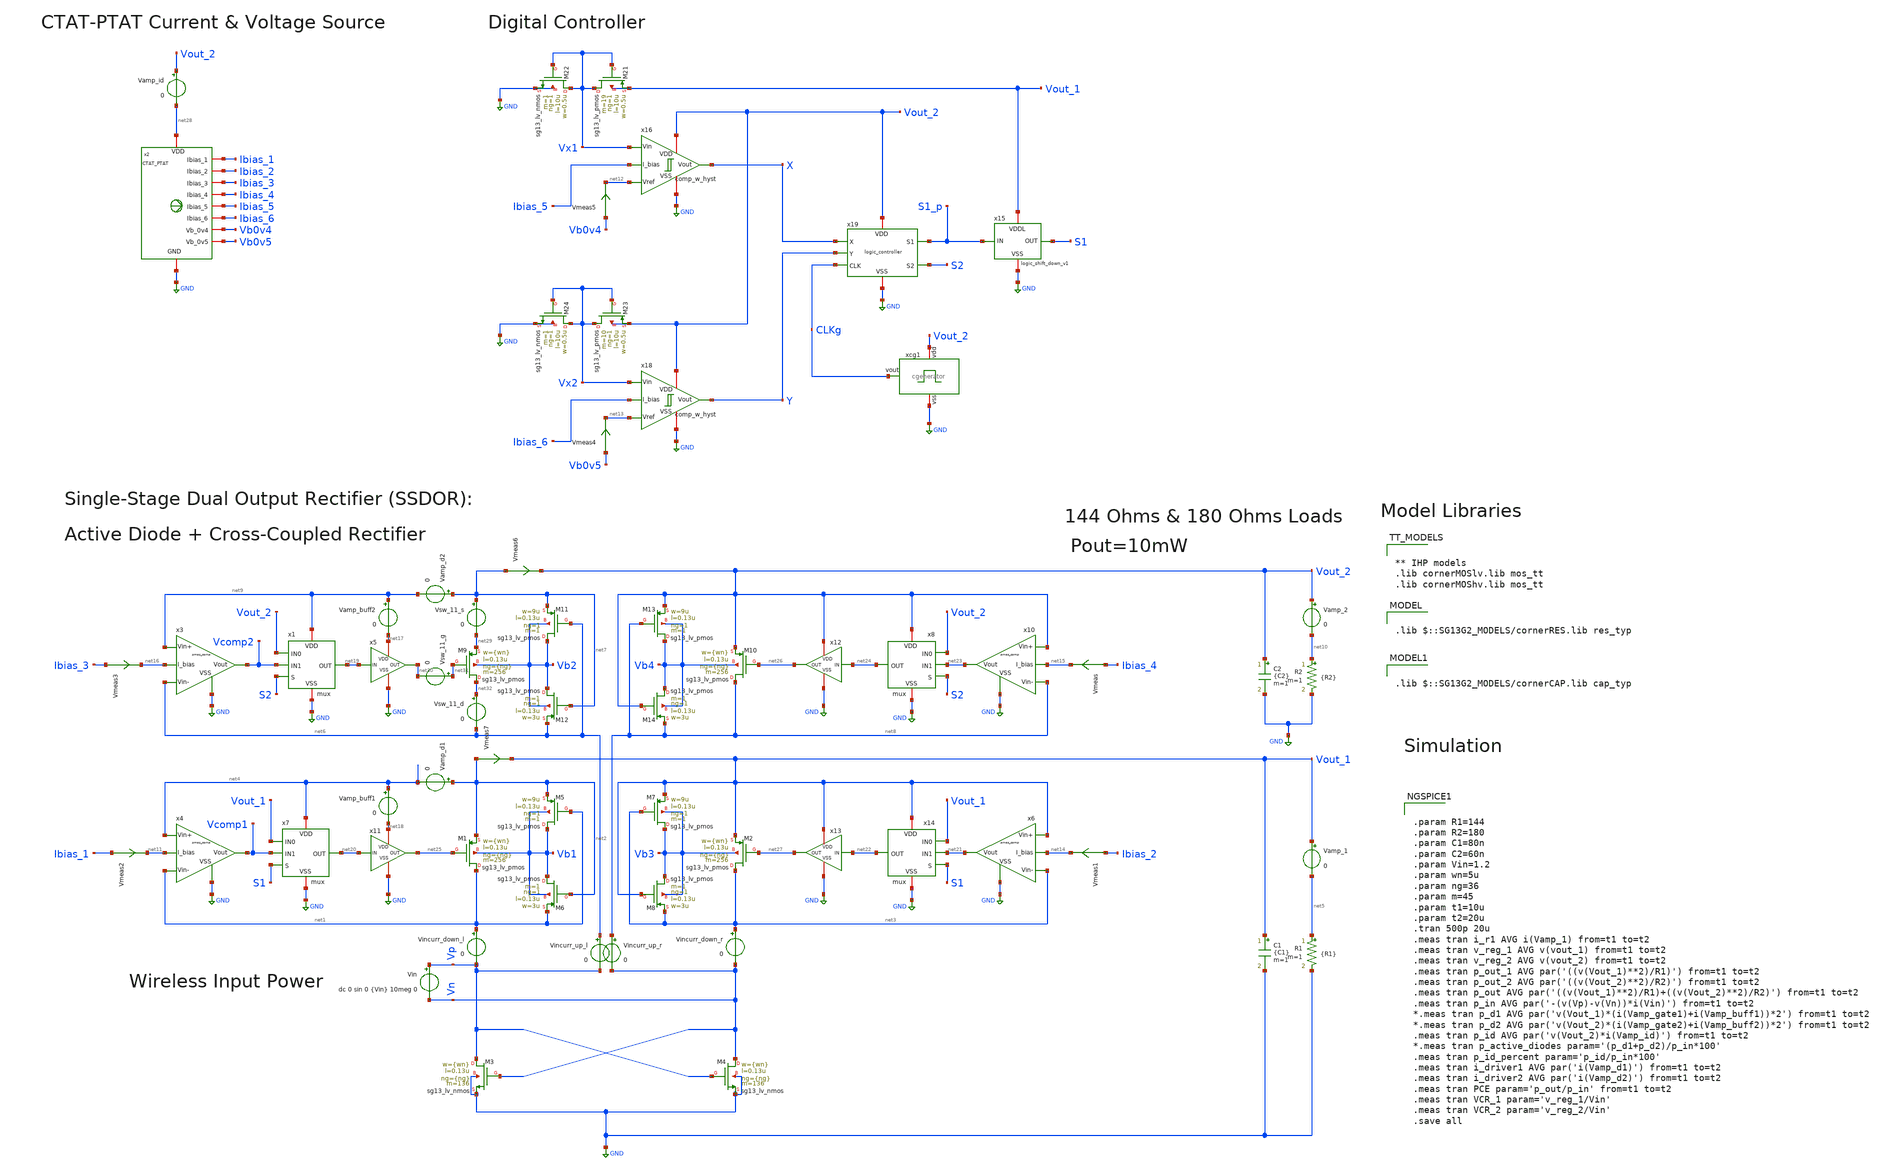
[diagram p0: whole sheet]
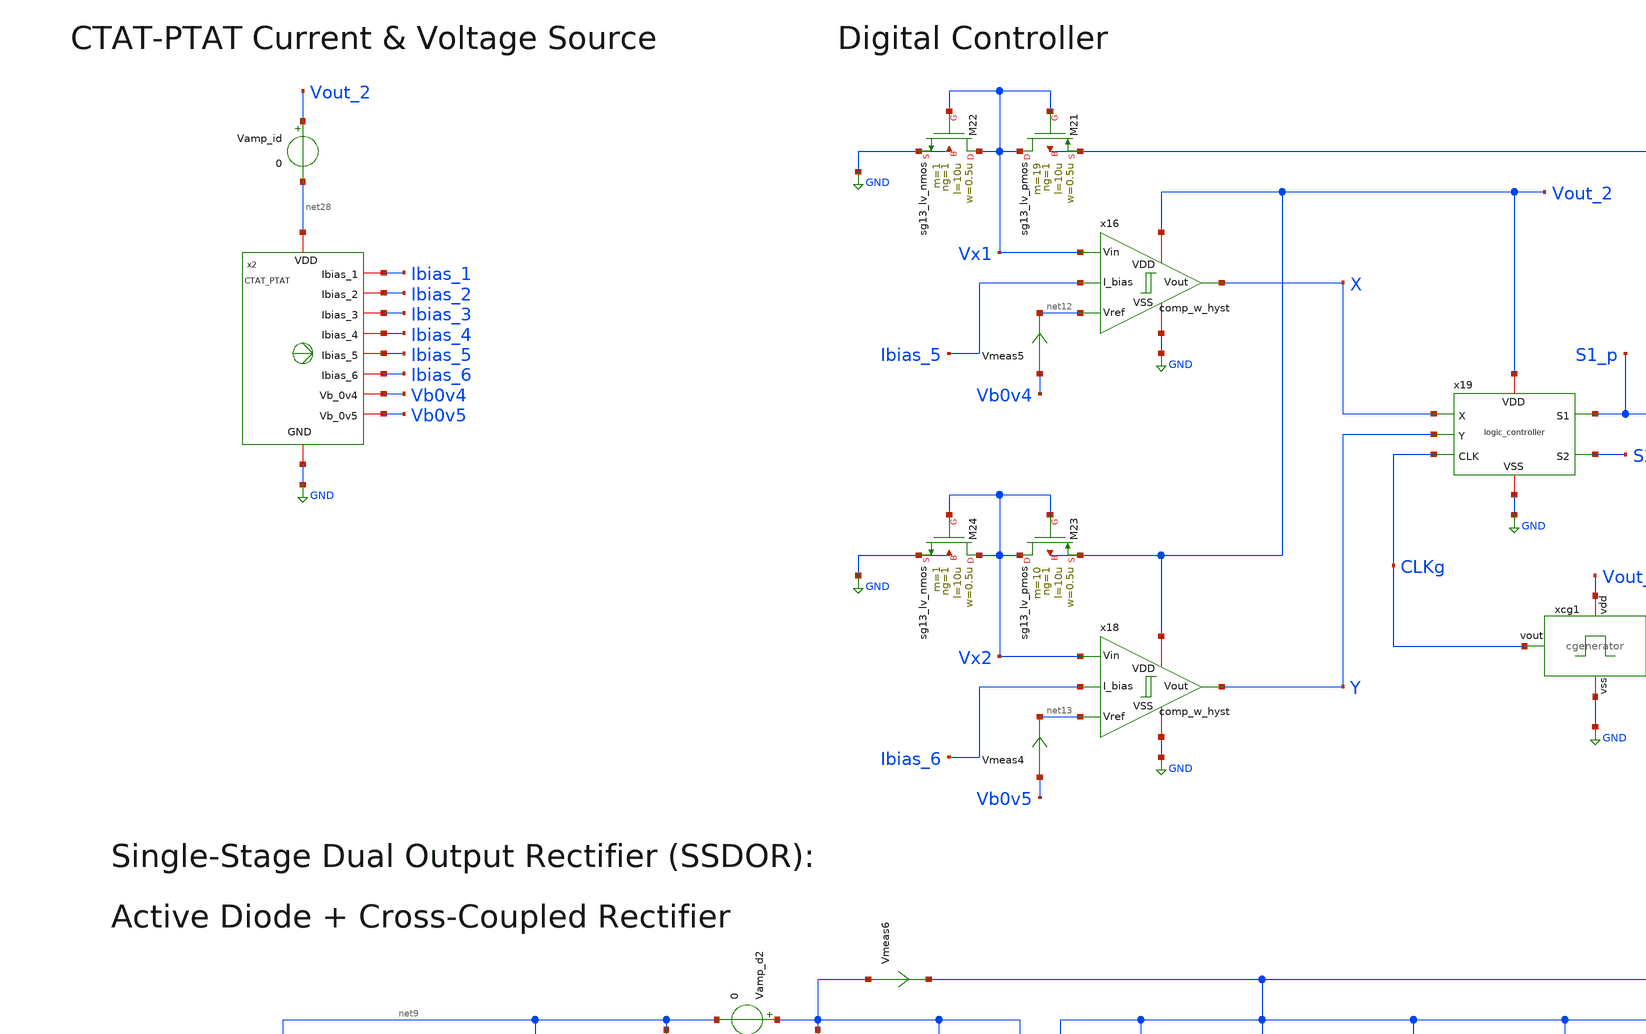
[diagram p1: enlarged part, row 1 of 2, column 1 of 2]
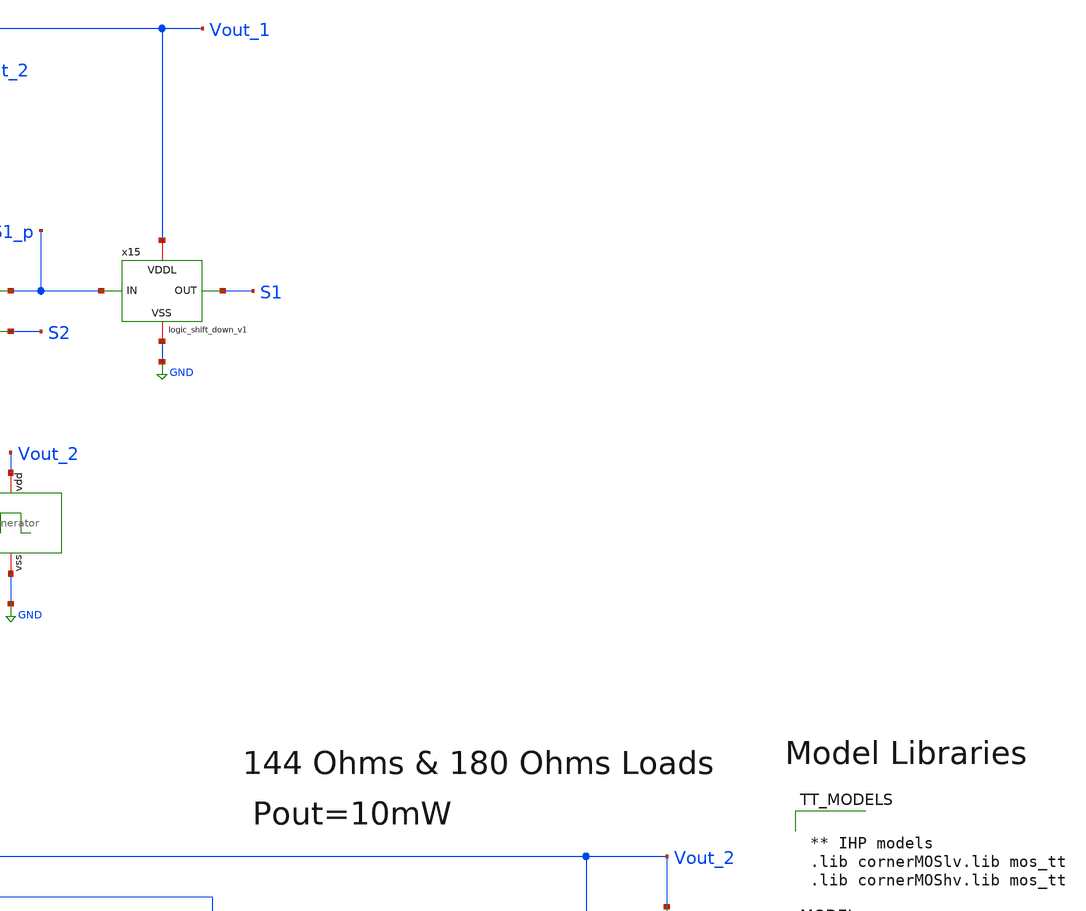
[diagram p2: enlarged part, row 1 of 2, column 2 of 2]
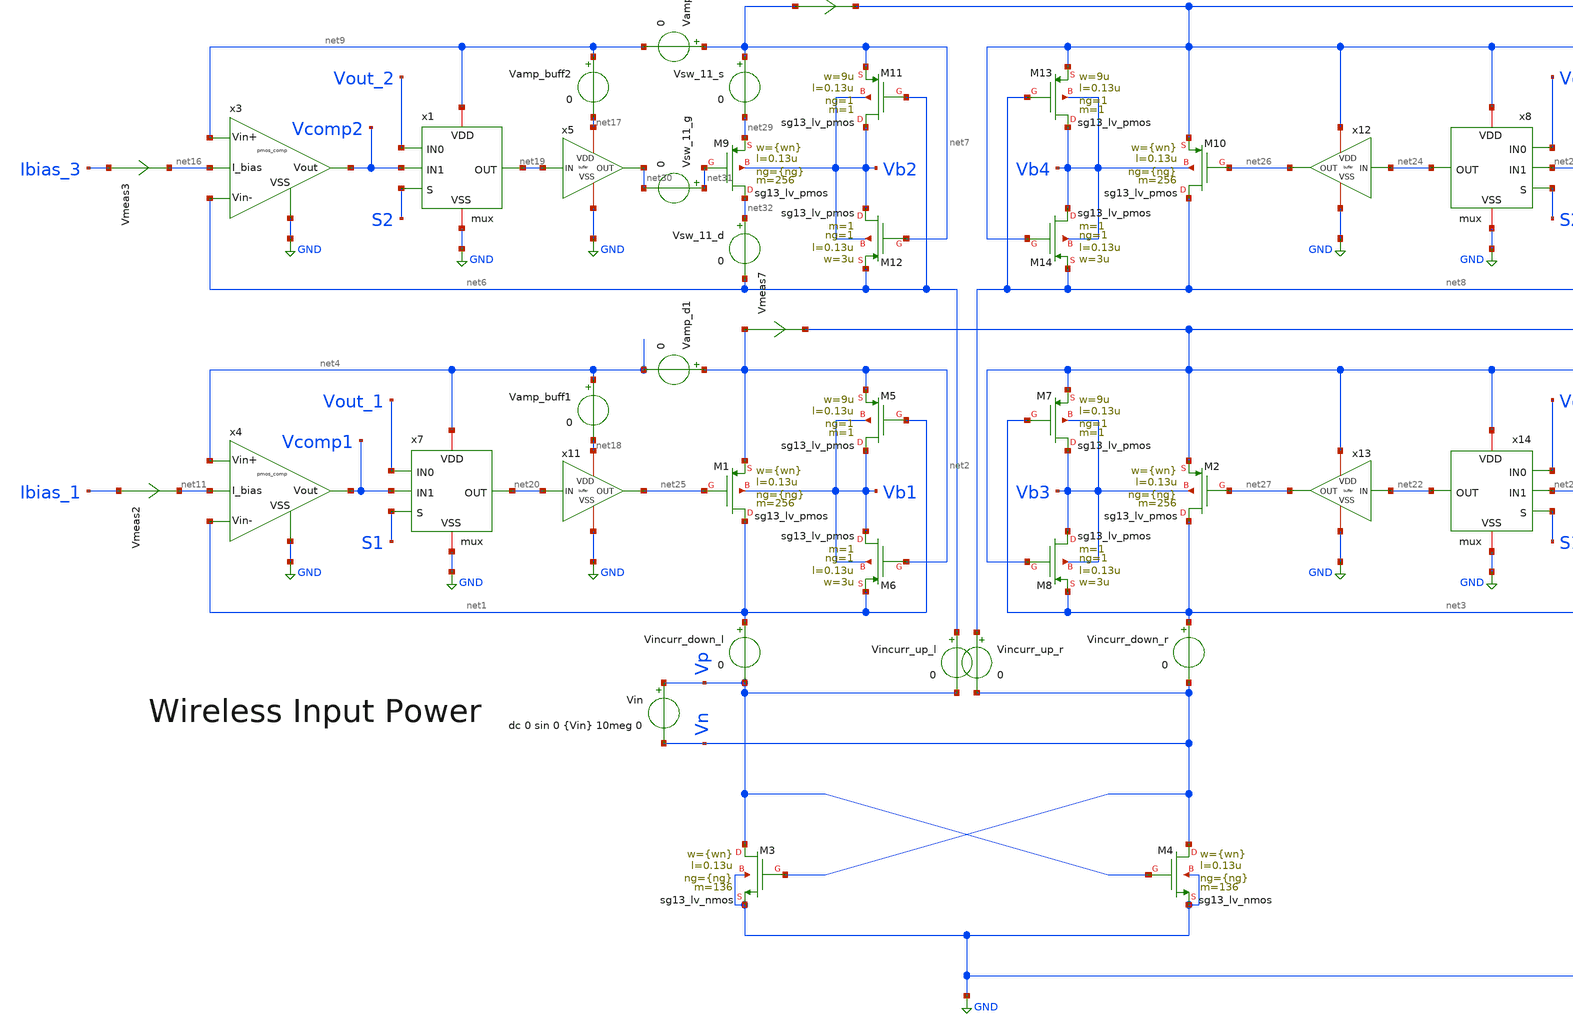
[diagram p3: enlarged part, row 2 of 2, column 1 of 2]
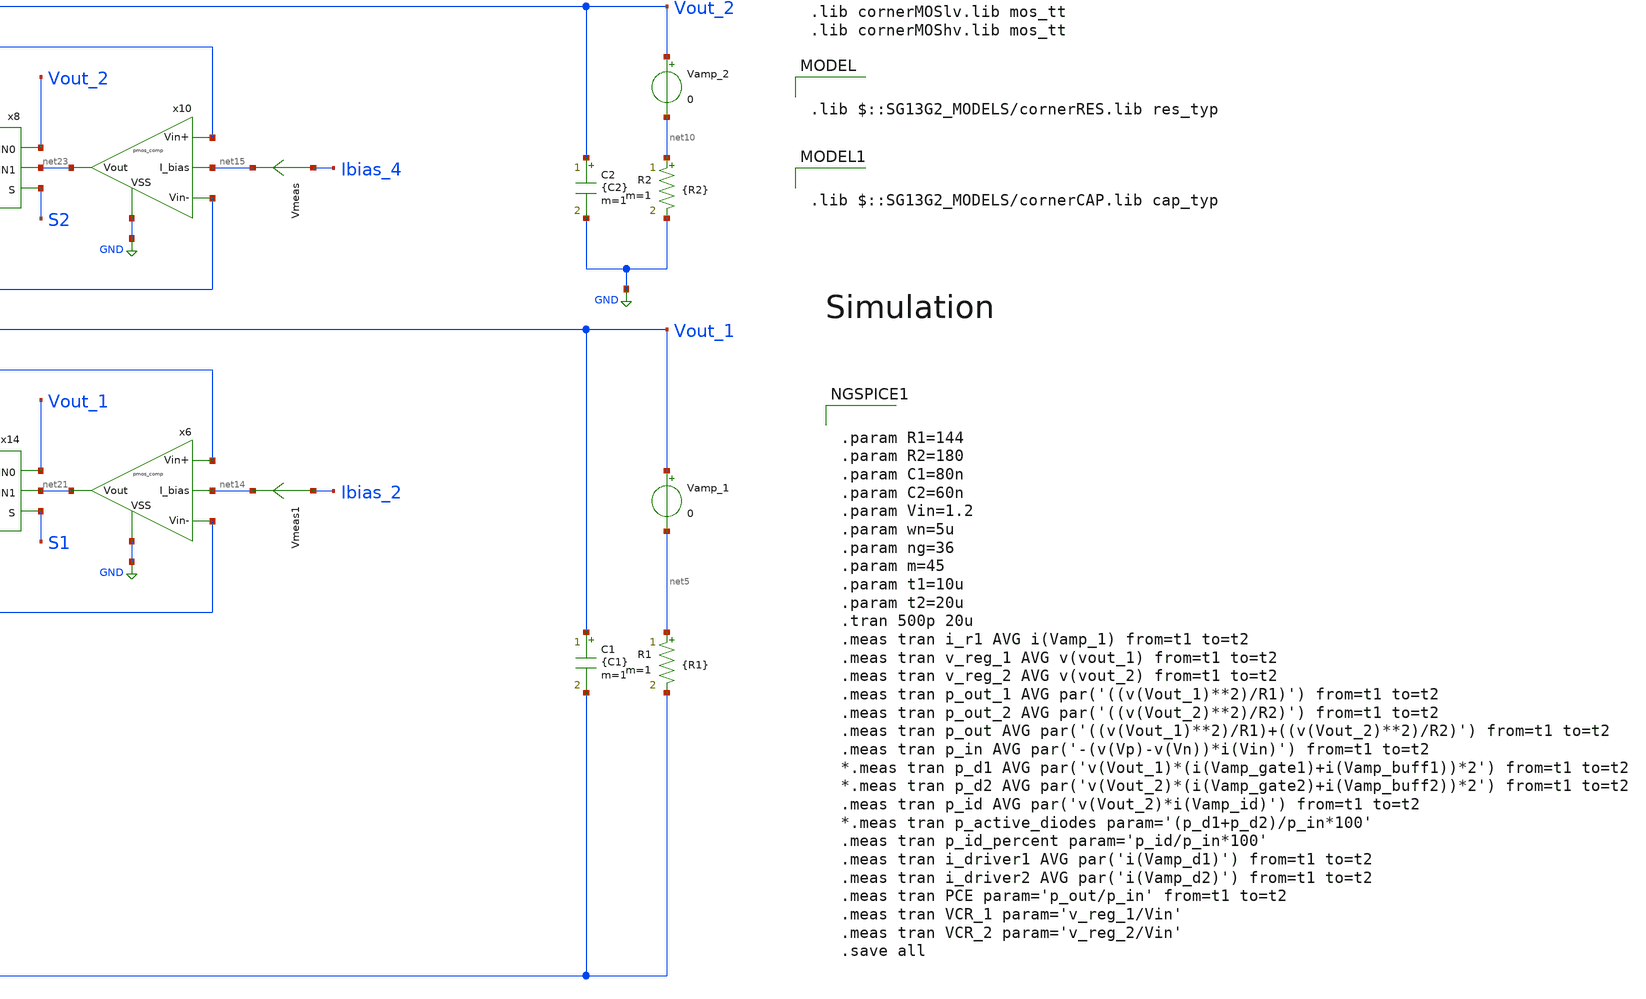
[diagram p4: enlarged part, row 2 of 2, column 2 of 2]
** sch_path: SSDOR_1.2V_v3/SSDOR_1.2V_v5_layout.sch
**.subckt SSDOR_1.2V_v5_layout
XM1 net1 net25 net2 Vb1 sg13_lv_pmos w={wn} l=0.13u ng={ng} m=256 mm_ok=1
XM2 net3 net27 Vout_1 Vb3 sg13_lv_pmos w={wn} l=0.13u ng={ng} m=256 mm_ok=1
XM3 Vp Vn GND GND sg13_lv_nmos w={wn} l=0.13u ng={ng} m=136 mm_ok=1
XM4 Vn Vp GND GND sg13_lv_nmos w={wn} l=0.13u ng={ng} m=136 mm_ok=1
XM5 Vb1 net1 net2 Vb1 sg13_lv_pmos w=9u l=0.13u ng=1 m=1 mm_ok=1
XM6 Vb1 net2 net1 Vb1 sg13_lv_pmos w=3u l=0.13u ng=1 m=1 mm_ok=1
XM7 Vb3 net3 Vout_1 Vb3 sg13_lv_pmos w=9u l=0.13u ng=1 m=1 mm_ok=1
XM8 Vb3 Vout_1 net3 Vb3 sg13_lv_pmos w=3u l=0.13u ng=1 m=1 mm_ok=1
Vin Vp Vn dc 0 sin 0 {Vin} 10meg 0
C1 Vout_1 GND {C1} m=1
R1 net5 GND {R1} m=1
Vamp_1 Vout_1 net5 0
XM9 net32 net31 net29 Vb2 sg13_lv_pmos w={wn} l=0.13u ng={ng} m=256 mm_ok=1
XM10 net8 net26 Vout_2 Vb4 sg13_lv_pmos w={wn} l=0.13u ng={ng} m=256 mm_ok=1
XM11 Vb2 net6 net7 Vb2 sg13_lv_pmos w=9u l=0.13u ng=1 m=1 mm_ok=1
XM12 Vb2 net7 net6 Vb2 sg13_lv_pmos w=3u l=0.13u ng=1 m=1 mm_ok=1
XM13 Vb4 net8 Vout_2 Vb4 sg13_lv_pmos w=9u l=0.13u ng=1 m=1 mm_ok=1
XM14 Vb4 Vout_2 net8 Vb4 sg13_lv_pmos w=3u l=0.13u ng=1 m=1 mm_ok=1
C2 Vout_2 GND {C2} m=1
R2 net10 GND {R2} m=1
Vamp_2 Vout_2 net10 0
XM21 Vx1 Vx1 Vout_1 Vout_1 sg13_lv_pmos w=0.5u l=10u ng=1 m=19 mm_ok=1
XM22 Vx1 Vx1 GND GND sg13_lv_nmos w=0.5u l=10u ng=1 m=1 mm_ok=1
XM23 Vx2 Vx2 Vout_2 Vout_2 sg13_lv_pmos w=0.5u l=10u ng=1 m=10 mm_ok=1
XM24 Vx2 Vx2 GND GND sg13_lv_nmos w=0.5u l=10u ng=1 m=1 mm_ok=1
Vamp_d2 net7 net9 0
Vamp_d1 net2 net4 0
Vamp_buff2 net9 net17 0
Vamp_buff1 net4 net18 0
Vmeas Ibias_4 net15 0
.save i(vmeas)
Vmeas1 Ibias_2 net14 0
.save i(vmeas1)
Vmeas2 Ibias_1 net11 0
.save i(vmeas2)
Vmeas3 Ibias_3 net16 0
.save i(vmeas3)
Vamp_id Vout_2 net28 0
x2 net28 GND Ibias_4 Ibias_1 Ibias_2 Ibias_5 Ibias_6 Ibias_3 Vb0v5 Vb0v4 CTAT_PTAT
x16 Vout_2 GND net12 Vx1 X Ibias_5 comp_w_hyst
x18 Vout_2 GND net13 Vx2 Y Ibias_6 comp_w_hyst
x19 Vout_2 X S1_p CLKg Y S2 GND logic_controller
x15 Vout_1 S1_p S1 GND logic_shift_down_v1
x3 net6 net9 Vcomp2 net16 GND pmos_comp
x4 net1 net4 Vcomp1 net11 GND pmos_comp
x6 net3 Vout_1 net21 net14 GND pmos_comp
x10 net8 Vout_2 net23 net15 GND pmos_comp
x1 net9 Vout_2 S2 net19 Vcomp2 GND mux
x7 net4 Vout_1 S1 net20 Vcomp1 GND mux
x8 Vout_2 Vout_2 S2 net24 net23 GND mux
x14 Vout_1 Vout_1 S1 net22 net21 GND mux
x5 net17 net19 net30 GND buffer wn=1u
x11 net18 net20 net25 GND buffer wn=1u
x12 Vout_2 net24 net26 GND buffer wn=1u
x13 Vout_1 net22 net27 GND buffer wn=1u
xcg1 Vout_2 CLKg GND cgenerator
Vsw_11_s net7 net29 0
Vsw_11_g net31 net30 0
Vsw_11_d net32 net6 0
Vincurr_up_l net6 Vp 0
Vincurr_up_r net8 Vn 0
Vincurr_down_l net1 Vp 0
Vincurr_down_r net3 Vn 0
Vmeas4 Vb0v5 net13 0
.save i(vmeas4)
Vmeas5 Vb0v4 net12 0
.save i(vmeas5)
Vmeas6 net7 Vout_2 0
.save i(vmeas6)
Vmeas7 net2 Vout_1 0
.save i(vmeas7)
**** begin user architecture code


** IHP models
.lib cornerMOSlv.lib mos_tt
.lib cornerMOShv.lib mos_tt



.lib $::SG13G2_MODELS/cornerRES.lib res_typ


.lib $::SG13G2_MODELS/cornerCAP.lib cap_typ



.param R1=144
.param R2=180
.param C1=80n
.param C2=60n
.param Vin=1.2
.param wn=5u
.param ng=36
.param m=45
.param t1=10u
.param t2=20u
.tran 500p 20u
.meas tran i_r1 AVG i(Vamp_1) from=t1 to=t2
.meas tran v_reg_1 AVG v(vout_1) from=t1 to=t2
.meas tran v_reg_2 AVG v(vout_2) from=t1 to=t2
.meas tran p_out_1 AVG par('((v(Vout_1)**2)/R1)') from=t1 to=t2
.meas tran p_out_2 AVG par('((v(Vout_2)**2)/R2)') from=t1 to=t2
.meas tran p_out AVG par('((v(Vout_1)**2)/R1)+((v(Vout_2)**2)/R2)') from=t1 to=t2
.meas tran p_in AVG par('-(v(Vp)-v(Vn))*i(Vin)') from=t1 to=t2
*.meas tran p_d1 AVG par('v(Vout_1)*(i(Vamp_gate1)+i(Vamp_buff1))*2') from=t1 to=t2
*.meas tran p_d2 AVG par('v(Vout_2)*(i(Vamp_gate2)+i(Vamp_buff2))*2') from=t1 to=t2
.meas tran p_id AVG par('v(Vout_2)*i(Vamp_id)') from=t1 to=t2
*.meas tran p_active_diodes param='(p_d1+p_d2)/p_in*100'
.meas tran p_id_percent param='p_id/p_in*100'
.meas tran i_driver1 AVG par('i(Vamp_d1)') from=t1 to=t2
.meas tran i_driver2 AVG par('i(Vamp_d2)') from=t1 to=t2
.meas tran PCE param='p_out/p_in' from=t1 to=t2
.meas tran VCR_1 param='v_reg_1/Vin'
.meas tran VCR_2 param='v_reg_2/Vin'
.save all


**** end user architecture code
**.ends
.GLOBAL GND
.end
